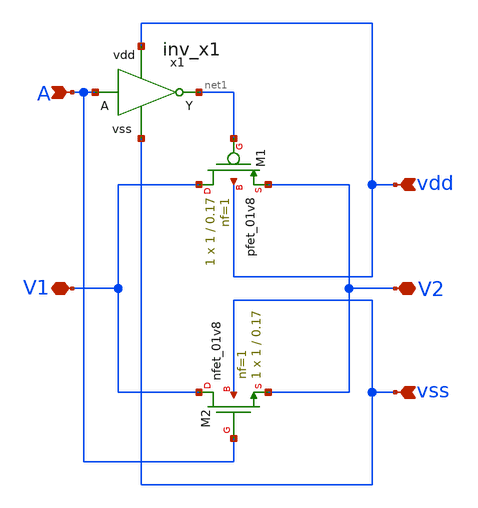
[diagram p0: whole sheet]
** sch_path: xschem/t-gate/t_gate.sch
**.subckt t_gate V1 V2 A vdd vss
*.iopin V1
*.iopin V2
*.ipin A
*.ipin vdd
*.ipin vss
XM2 V1 A V2 vss sky130_fd_pr__nfet_01v8 L=0.17 W=1 nf=1 ad={int((nf+1)/2) * W/nf * 0.29} as={int((nf+2)/2) * W/nf * 0.29}
+ pd={2*int((nf+1)/2) * (W/nf + 0.29)} ps={2*int((nf+2)/2) * (W/nf + 0.29)} nrd={0.29 / W} nrs={0.29 / W}
+ sa=0 sb=0 sd=0 mult=1 m=1
XM1 V1 net1 V2 vdd sky130_fd_pr__pfet_01v8 L=0.17 W=1 nf=1 ad={int((nf+1)/2) * W/nf * 0.29} as={int((nf+2)/2) * W/nf * 0.29}
+ pd={2*int((nf+1)/2) * (W/nf + 0.29)} ps={2*int((nf+2)/2) * (W/nf + 0.29)} nrd={0.29 / W} nrs={0.29 / W}
+ sa=0 sb=0 sd=0 mult=1 m=1
x1 vdd net1 A vss inv_x1
**.ends
.end
